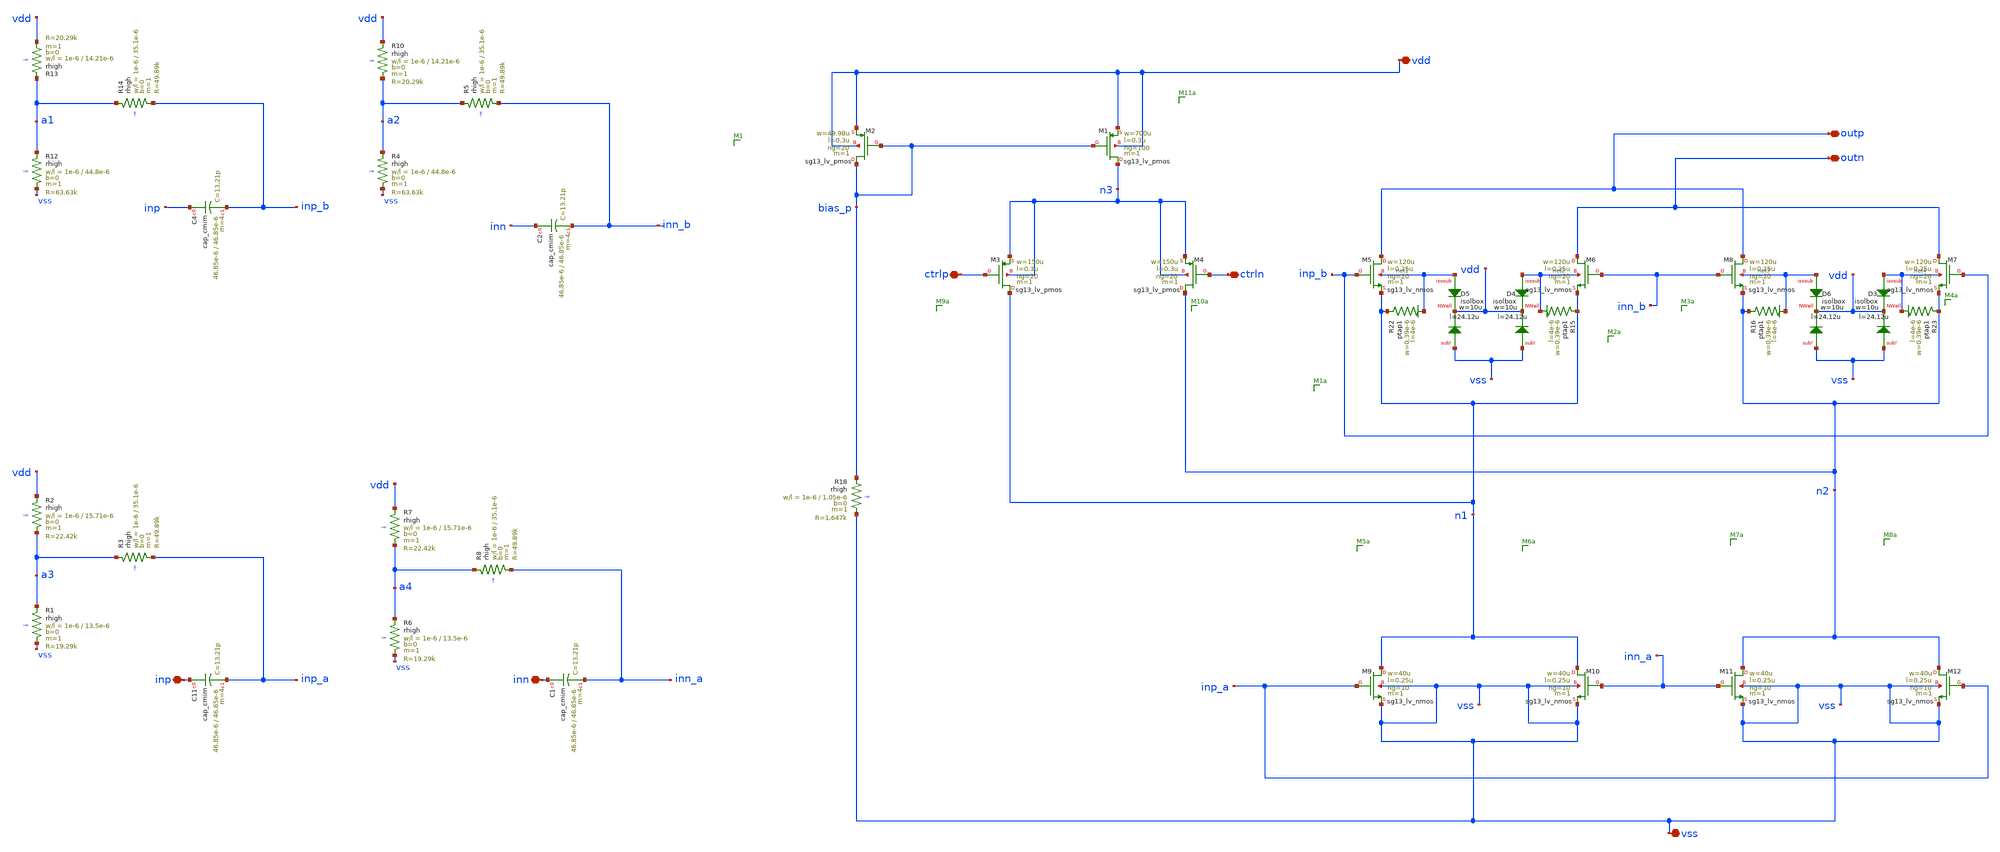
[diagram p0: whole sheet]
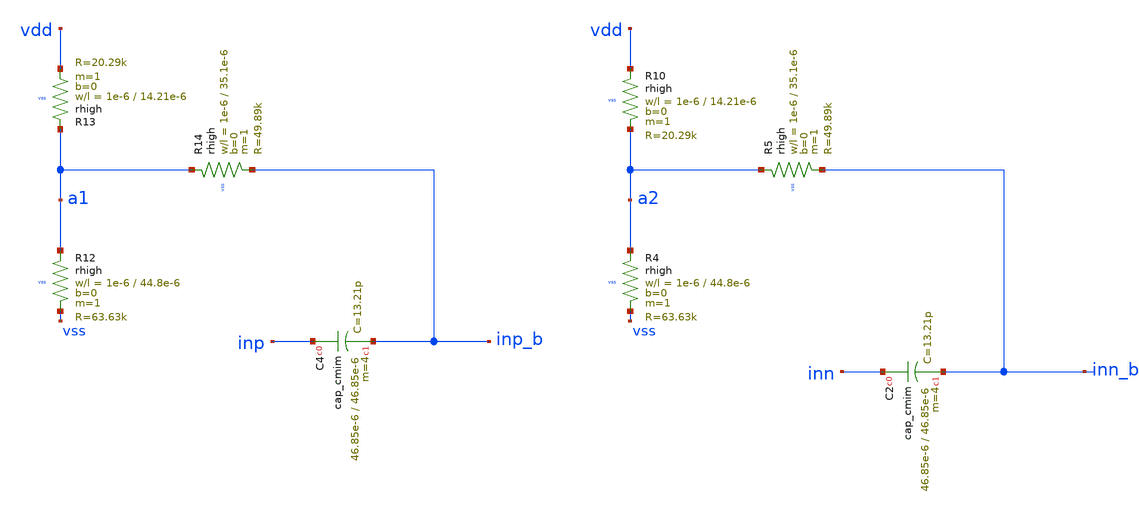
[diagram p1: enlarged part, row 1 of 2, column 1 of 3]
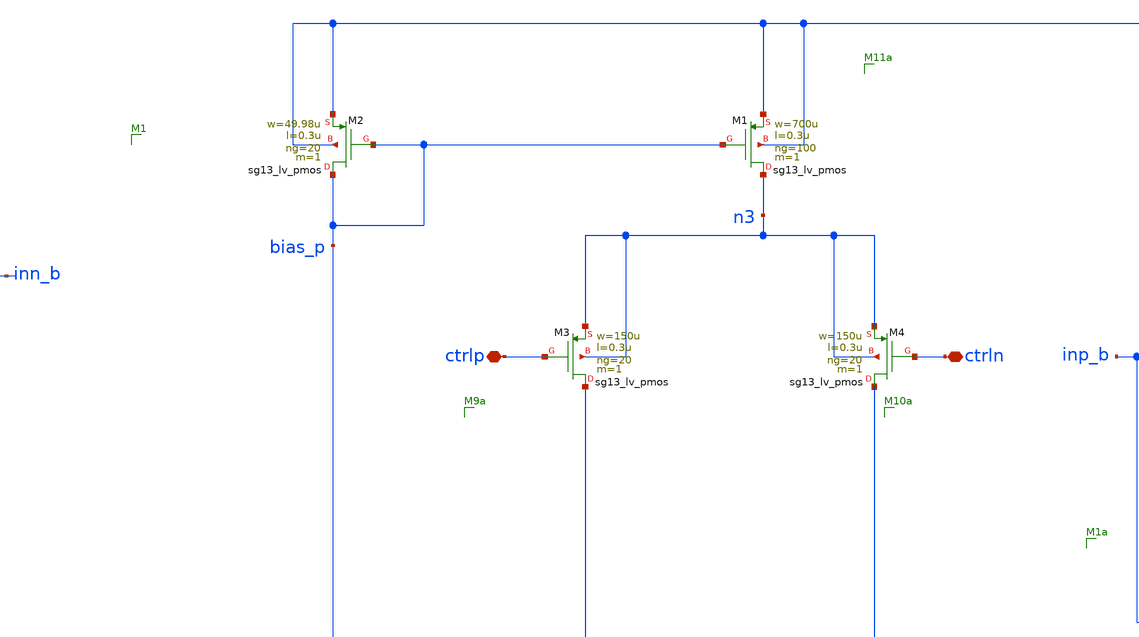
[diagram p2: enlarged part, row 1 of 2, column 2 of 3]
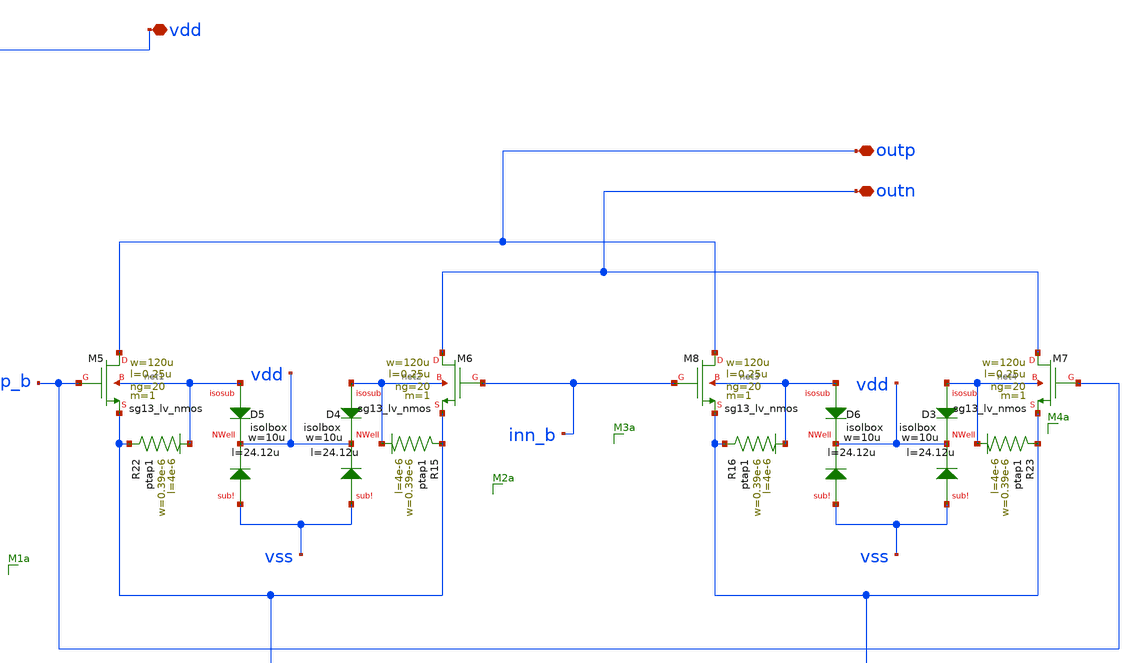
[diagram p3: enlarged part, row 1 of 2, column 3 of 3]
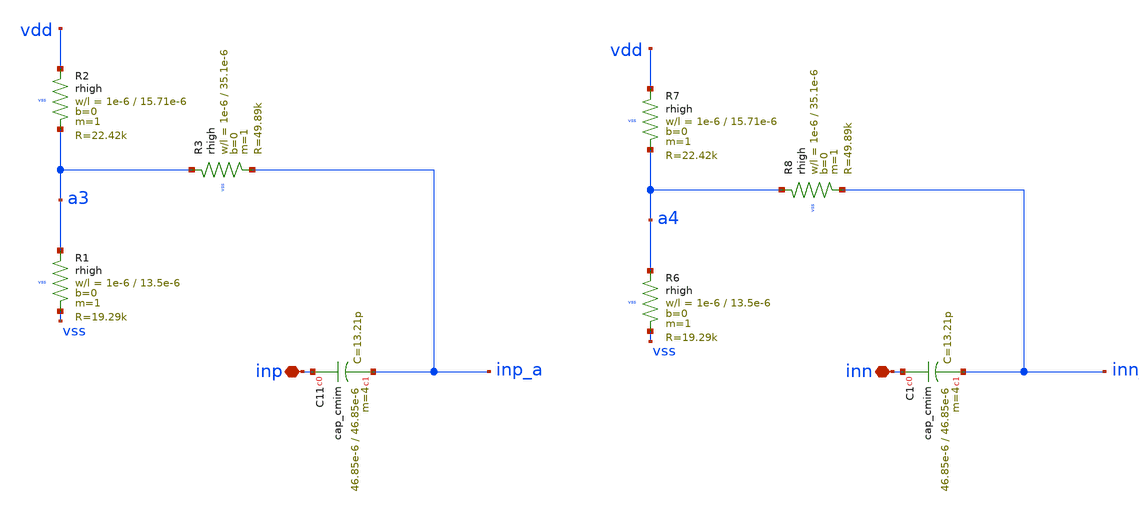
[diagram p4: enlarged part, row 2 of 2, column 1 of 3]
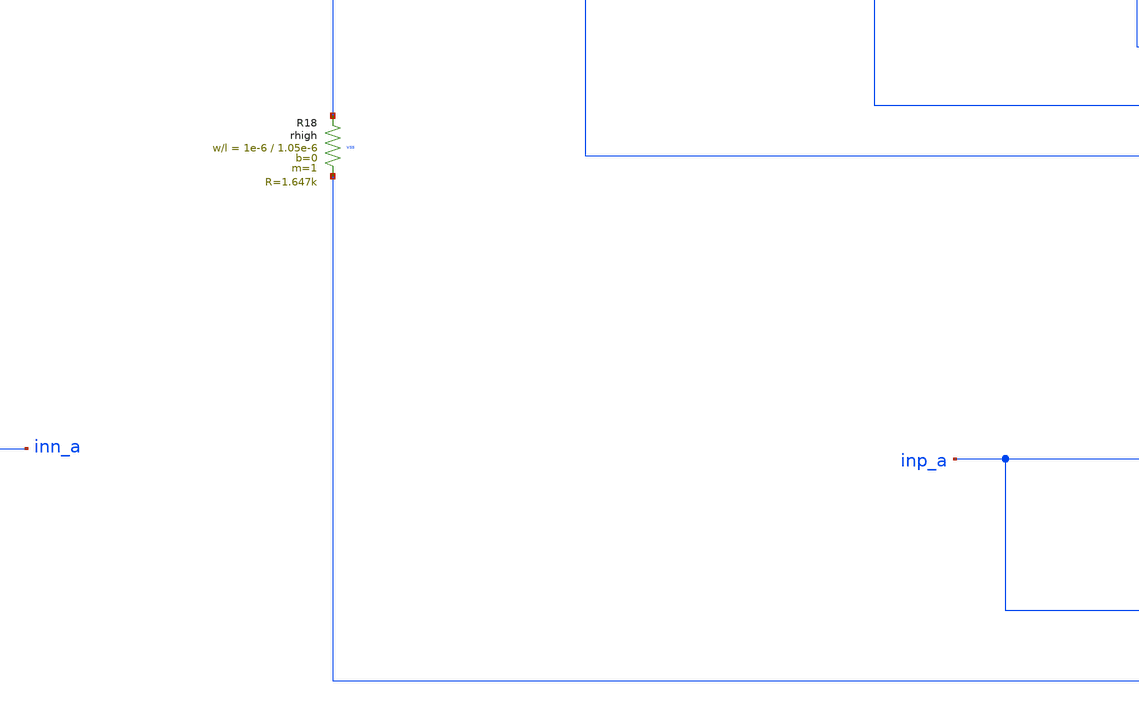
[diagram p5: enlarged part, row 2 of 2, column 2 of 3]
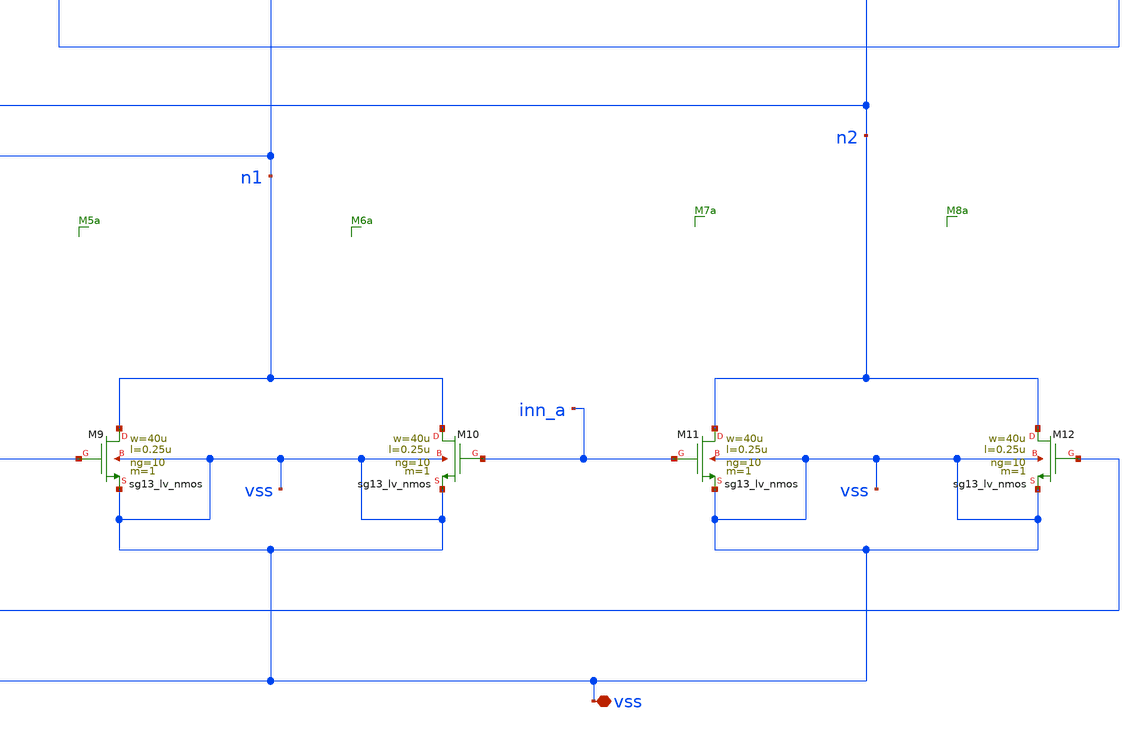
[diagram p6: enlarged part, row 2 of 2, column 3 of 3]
** sch_path: LNA7096-main/schematic/xschem/05_vga/vga_sch_I.sch
**.subckt vga_sch_I vdd vss inp outp outn ctrlp ctrln inn
*.iopin vdd
*.iopin vss
*.iopin inp
*.iopin outp
*.iopin outn
*.iopin ctrlp
*.iopin ctrln
*.iopin inn
XR7 vdd a4 vss rhigh w=1e-6 l=15.71e-6 m=1 b=0 mm_ok=1
XR1 a3 vss vss rhigh w=1e-6 l=13.5e-6 m=1 b=0 mm_ok=1
XR2 vdd a3 vss rhigh w=1e-6 l=15.71e-6 m=1 b=0 mm_ok=1
XR10 vdd a2 vss rhigh w=1e-6 l=14.21e-6 m=1 b=0 mm_ok=1
XR12 a1 vss vss rhigh w=1e-6 l=44.8e-6 m=1 b=0 mm_ok=1
XR13 a1 vdd vss rhigh w=1e-6 l=14.21e-6 m=1 b=0 mm_ok=1
XC4 inp inp_b cap_cmim w=46.85e-6 l=46.85e-6 m=4 mm_ok=1
XR14 a1 inp_b vss rhigh w=1e-6 l=35.1e-6 m=1 b=0 mm_ok=1
XR18 bias_p vss vss rhigh w=1e-6 l=1.05e-6 m=1 b=0 mm_ok=1
XC2 inn inn_b cap_cmim w=46.85e-6 l=46.85e-6 m=4 mm_ok=1
XC11 inp inp_a cap_cmim w=46.85e-6 l=46.85e-6 m=4 mm_ok=1
XC1 inn inn_a cap_cmim w=46.85e-6 l=46.85e-6 m=4 mm_ok=1
XM2 bias_p bias_p vdd vdd sg13_lv_pmos w=49.98u l=0.3u ng=20 m=1 mm_ok=1
XM1 n3 bias_p vdd vdd sg13_lv_pmos w=700u l=0.3u ng=100 m=1 mm_ok=1
XM3 n1 ctrlp n3 n3 sg13_lv_pmos w=150u l=0.3u ng=20 m=1 mm_ok=1
XM4 n2 ctrln n3 n3 sg13_lv_pmos w=150u l=0.3u ng=20 m=1 mm_ok=1
XM5 outp inp_b n1 net1 sg13_lv_nmos w=120u l=0.25u ng=20 m=1 mm_ok=1
XM6 outn inn_b n1 net2 sg13_lv_nmos w=120u l=0.25u ng=20 m=1 mm_ok=1
XM7 outn inp_b n2 net4 sg13_lv_nmos w=120u l=0.25u ng=20 m=1 mm_ok=1
XM8 outp inn_b n2 net3 sg13_lv_nmos w=120u l=0.25u ng=20 m=1 mm_ok=1
XM9 n1 inp_a vss vss sg13_lv_nmos w=40u l=0.25u ng=10 m=1 mm_ok=1
XM10 n1 inn_a vss vss sg13_lv_nmos w=40u l=0.25u ng=10 m=1 mm_ok=1
XM11 n2 inn_a vss vss sg13_lv_nmos w=40u l=0.25u ng=10 m=1 mm_ok=1
XM12 n2 inp_a vss vss sg13_lv_nmos w=40u l=0.25u ng=10 m=1 mm_ok=1
XD4 net2 vdd vss isolbox l=24.12u w=10u
XD5 net1 vdd vss isolbox l=24.12u w=10u
XR22 n1 net1 ptap1 R=94.78 w=0.39e-6 l=4e-6
XR15 n1 net2 ptap1 R=94.78 w=0.39e-6 l=4e-6
XD3 net4 vdd vss isolbox l=24.12u w=10u
XD6 net3 vdd vss isolbox l=24.12u w=10u
XR16 n2 net3 ptap1 R=94.78 w=0.39e-6 l=4e-6
XR23 n2 net4 ptap1 R=94.78 w=0.39e-6 l=4e-6
XR4 a2 vss vss rhigh w=1e-6 l=44.8e-6 m=1 b=0 mm_ok=1
XR5 a2 inn_b vss rhigh w=1e-6 l=35.1e-6 m=1 b=0 mm_ok=1
XR6 a4 vss vss rhigh w=1e-6 l=13.5e-6 m=1 b=0 mm_ok=1
XR3 a3 inp_a vss rhigh w=1e-6 l=35.1e-6 m=1 b=0 mm_ok=1
XR8 a4 inn_a vss rhigh w=1e-6 l=35.1e-6 m=1 b=0 mm_ok=1
**.ends
.end
